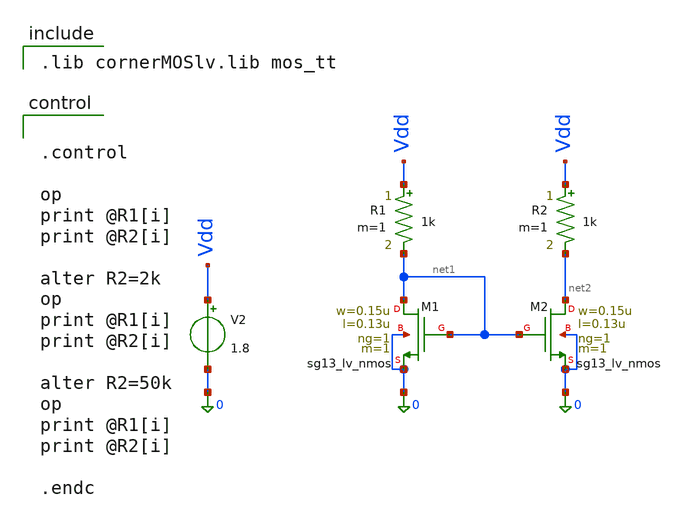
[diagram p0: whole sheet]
** sch_path: designs/current mirror/current_mirror.sch
**.subckt current_mirror
V2 Vdd 0 1.8
XM2 net2 net1 0 0 sg13_lv_nmos w=0.15u l=0.13u ng=1 m=1 mm_ok=1
XM1 net1 net1 0 0 sg13_lv_nmos w=0.15u l=0.13u ng=1 m=1 mm_ok=1
R1 Vdd net1 1k m=1
R2 Vdd net2 1k m=1
**** begin user architecture code

.lib cornerMOSlv.lib mos_tt



.control

op
print @R1[i]
print @R2[i]

alter R2=2k
op
print @R1[i]
print @R2[i]

alter R2=50k
op
print @R1[i]
print @R2[i]

.endc


**** end user architecture code
**.ends
.end
